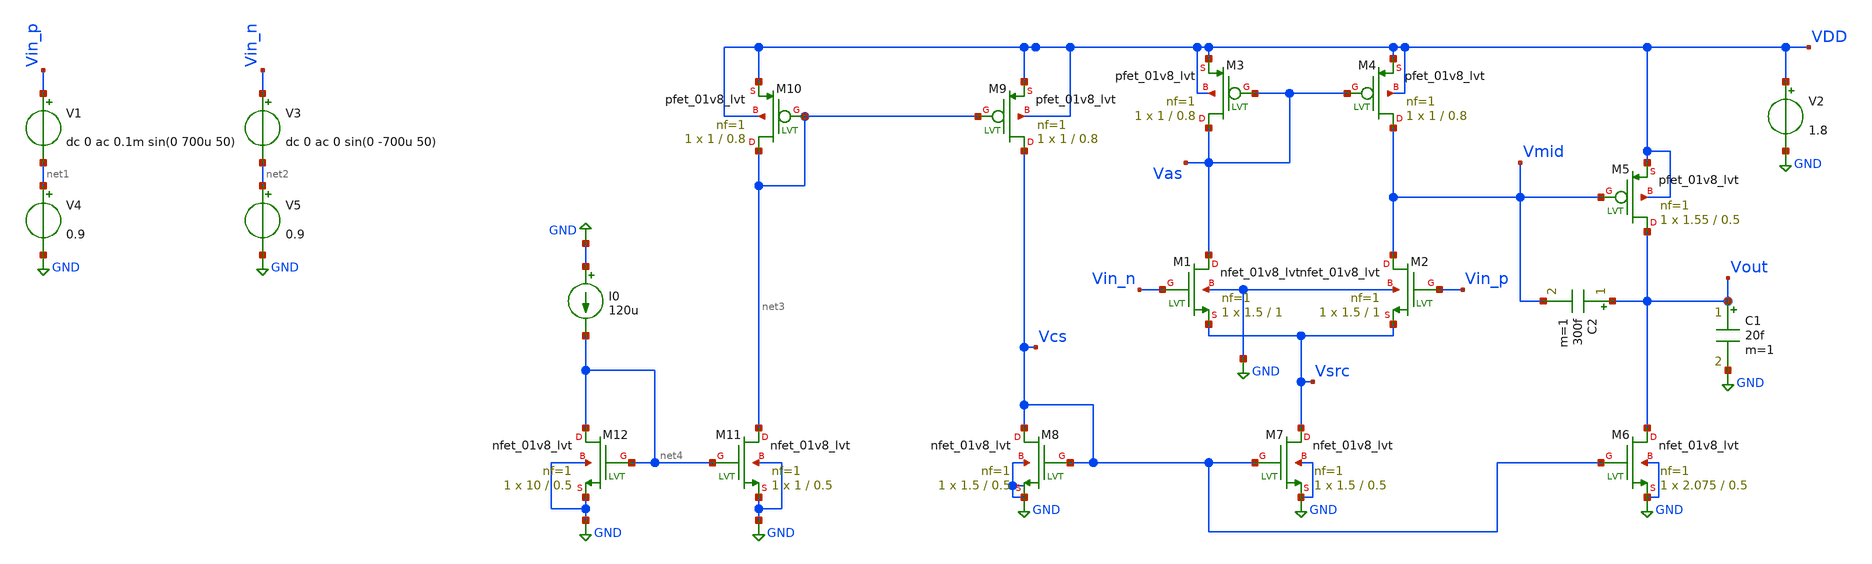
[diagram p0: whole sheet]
** sch_path: xchem/OTA3_lvt.sch
* Copyright 2021 Stefan Frederik Schippers
* Licensed under the Apache License, Version 2.0 (the "License");
* you may not use this file except in compliance with the License.
* You may obtain a copy of the License at
* https://www.apache.org/licenses/LICENSE-2.0
* Unless required by applicable law or agreed to in writing, software
* distributed under the License is distributed on an "AS IS" BASIS,
* WITHOUT WARRANTIES OR CONDITIONS OF ANY KIND, either express or implied.
* See the License for the specific language governing permissions and
* limitations under the License.
**.subckt OTA3_lvt
C1 Vout GND 20f m=1
V2 VDD GND 1.8
V1 Vin_p net1 dc 0 ac 0.1m sin(0 700u 50)
V3 Vin_n net2 dc 0 ac 0 sin(0 -700u 50)
V4 net1 GND 0.9
V5 net2 GND 0.9
XM1 Vas Vin_n Vsrc GND sky130_fd_pr__nfet_01v8_lvt L=1 W=1.5 nf=1 ad='int((nf+1)/2) * W/nf * 0.29' as='int((nf+2)/2) * W/nf * 0.29'
+ pd='2*int((nf+1)/2) * (W/nf + 0.29)' ps='2*int((nf+2)/2) * (W/nf + 0.29)' nrd='0.29 / W' nrs='0.29 / W'
+ sa=0 sb=0 sd=0 mult=1 m=1
XM2 Vmid Vin_p Vsrc GND sky130_fd_pr__nfet_01v8_lvt L=1 W=1.5 nf=1 ad='int((nf+1)/2) * W/nf * 0.29' as='int((nf+2)/2) * W/nf * 0.29'
+ pd='2*int((nf+1)/2) * (W/nf + 0.29)' ps='2*int((nf+2)/2) * (W/nf + 0.29)' nrd='0.29 / W' nrs='0.29 / W'
+ sa=0 sb=0 sd=0 mult=1 m=1
XM3 Vas Vas VDD VDD sky130_fd_pr__pfet_01v8_lvt L=0.8 W=1 nf=1 ad='int((nf+1)/2) * W/nf * 0.29' as='int((nf+2)/2) * W/nf * 0.29'
+ pd='2*int((nf+1)/2) * (W/nf + 0.29)' ps='2*int((nf+2)/2) * (W/nf + 0.29)' nrd='0.29 / W' nrs='0.29 / W'
+ sa=0 sb=0 sd=0 mult=1 m=1
XM4 Vmid Vas VDD VDD sky130_fd_pr__pfet_01v8_lvt L=0.8 W=1 nf=1 ad='int((nf+1)/2) * W/nf * 0.29' as='int((nf+2)/2) * W/nf * 0.29'
+ pd='2*int((nf+1)/2) * (W/nf + 0.29)' ps='2*int((nf+2)/2) * (W/nf + 0.29)' nrd='0.29 / W' nrs='0.29 / W'
+ sa=0 sb=0 sd=0 mult=1 m=1
XM5 Vout Vmid VDD VDD sky130_fd_pr__pfet_01v8_lvt L=0.5 W=1.55 nf=1 ad='int((nf+1)/2) * W/nf * 0.29'
+ as='int((nf+2)/2) * W/nf * 0.29' pd='2*int((nf+1)/2) * (W/nf + 0.29)' ps='2*int((nf+2)/2) * (W/nf + 0.29)'
+ nrd='0.29 / W' nrs='0.29 / W' sa=0 sb=0 sd=0 mult=1 m=1
XM6 Vout Vcs GND GND sky130_fd_pr__nfet_01v8_lvt L=0.5 W=2.075 nf=1 ad='int((nf+1)/2) * W/nf * 0.29'
+ as='int((nf+2)/2) * W/nf * 0.29' pd='2*int((nf+1)/2) * (W/nf + 0.29)' ps='2*int((nf+2)/2) * (W/nf + 0.29)'
+ nrd='0.29 / W' nrs='0.29 / W' sa=0 sb=0 sd=0 mult=1 m=1
XM7 Vsrc Vcs GND GND sky130_fd_pr__nfet_01v8_lvt L=0.5 W=1.5 nf=1 ad='int((nf+1)/2) * W/nf * 0.29' as='int((nf+2)/2) * W/nf * 0.29'
+ pd='2*int((nf+1)/2) * (W/nf + 0.29)' ps='2*int((nf+2)/2) * (W/nf + 0.29)' nrd='0.29 / W' nrs='0.29 / W'
+ sa=0 sb=0 sd=0 mult=1 m=1
XM8 Vcs Vcs GND GND sky130_fd_pr__nfet_01v8_lvt L=0.5 W=1.5 nf=1 ad='int((nf+1)/2) * W/nf * 0.29' as='int((nf+2)/2) * W/nf * 0.29'
+ pd='2*int((nf+1)/2) * (W/nf + 0.29)' ps='2*int((nf+2)/2) * (W/nf + 0.29)' nrd='0.29 / W' nrs='0.29 / W'
+ sa=0 sb=0 sd=0 mult=1 m=1
XM9 Vcs net3 VDD VDD sky130_fd_pr__pfet_01v8_lvt L=0.8 W=1 nf=1 ad='int((nf+1)/2) * W/nf * 0.29' as='int((nf+2)/2) * W/nf * 0.29'
+ pd='2*int((nf+1)/2) * (W/nf + 0.29)' ps='2*int((nf+2)/2) * (W/nf + 0.29)' nrd='0.29 / W' nrs='0.29 / W'
+ sa=0 sb=0 sd=0 mult=1 m=1
C2 Vout Vmid 300f m=1
XM10 net3 net3 VDD VDD sky130_fd_pr__pfet_01v8_lvt L=0.8 W=1 nf=1 ad='int((nf+1)/2) * W/nf * 0.29' as='int((nf+2)/2) * W/nf * 0.29'
+ pd='2*int((nf+1)/2) * (W/nf + 0.29)' ps='2*int((nf+2)/2) * (W/nf + 0.29)' nrd='0.29 / W' nrs='0.29 / W'
+ sa=0 sb=0 sd=0 mult=1 m=1
XM11 net3 net4 GND GND sky130_fd_pr__nfet_01v8_lvt L=0.5 W=1 nf=1 ad='int((nf+1)/2) * W/nf * 0.29' as='int((nf+2)/2) * W/nf * 0.29'
+ pd='2*int((nf+1)/2) * (W/nf + 0.29)' ps='2*int((nf+2)/2) * (W/nf + 0.29)' nrd='0.29 / W' nrs='0.29 / W'
+ sa=0 sb=0 sd=0 mult=1 m=1
XM12 net4 net4 GND GND sky130_fd_pr__nfet_01v8_lvt L=0.5 W=10 nf=1 ad='int((nf+1)/2) * W/nf * 0.29' as='int((nf+2)/2) * W/nf * 0.29'
+ pd='2*int((nf+1)/2) * (W/nf + 0.29)' ps='2*int((nf+2)/2) * (W/nf + 0.29)' nrd='0.29 / W' nrs='0.29 / W'
+ sa=0 sb=0 sd=0 mult=1 m=1
I0 GND net4 120u
**** begin user architecture code


.control
run
save all
*tran 10u 100m
*plot Vout
ac dec 101 1 1g
plot db(1*V(Vout)/(V(Vin_p) - V(Vin_n))), 180/PI*phase(V(Vout))


let id1  = @m.xm1.msky130_fd_pr__nfet_01v8_lvt[id]
let id2  = @m.xm2.msky130_fd_pr__nfet_01v8_lvt[id]
let id3  = @m.xm3.msky130_fd_pr__pfet_01v8_lvt[id]
let id4  = @m.xm4.msky130_fd_pr__pfet_01v8_lvt[id]
let id5  = @m.xm5.msky130_fd_pr__pfet_01v8_lvt[id]
let id6  = @m.xm6.msky130_fd_pr__nfet_01v8_lvt[id]
let id7  = @m.xm7.msky130_fd_pr__nfet_01v8_lvt[id]
let id8  = @m.xm8.msky130_fd_pr__nfet_01v8_lvt[id]

let gm1  = @m.xm1.msky130_fd_pr__nfet_01v8_lvt[gm]
let gm2  = @m.xm2.msky130_fd_pr__nfet_01v8_lvt[gm]
let gm3  = @m.xm3.msky130_fd_pr__pfet_01v8_lvt[gm]
let gm4  = @m.xm4.msky130_fd_pr__pfet_01v8_lvt[gm]
let gm5  = @m.xm5.msky130_fd_pr__pfet_01v8_lvt[gm]
let gm6  = @m.xm6.msky130_fd_pr__nfet_01v8_lvt[gm]
let gm7  = @m.xm7.msky130_fd_pr__nfet_01v8_lvt[gm]
let gm8  = @m.xm8.msky130_fd_pr__nfet_01v8_lvt[gm]

let gds1  = @m.xm1.msky130_fd_pr__nfet_01v8_lvt[gds]
let gds2  = @m.xm2.msky130_fd_pr__nfet_01v8_lvt[gds]
let gds3  = @m.xm3.msky130_fd_pr__pfet_01v8_lvt[gds]
let gds4  = @m.xm4.msky130_fd_pr__pfet_01v8_lvt[gds]
let gds5  = @m.xm5.msky130_fd_pr__pfet_01v8_lvt[gds]
let gds6  = @m.xm6.msky130_fd_pr__nfet_01v8_lvt[gds]

let Av1  = gm2/(gds2+gds4)
let Av2  = gm5/(gds5 + gds6)
let Av = Av1*Av2

let Cl = 20e-15
let Cn5 = @m.xm5.msky130_fd_pr__pfet_01v8_lvt[cgs]
let GBW = gm1/(6.28*(Cl + Cn5))

print gm1/id1
print gm2/id2
print gm3/id3
print gm4/id4
print gm5/id5
print gm6/id6
print gm7/id7
print gm8/id8

print Av1
print Av2
print Av
print GBW

.endc



** opencircuitdesign pdks install
.lib $::SKYWATER_MODELS/sky130.lib.spice tt


**** end user architecture code
**.ends
.GLOBAL GND
.end
